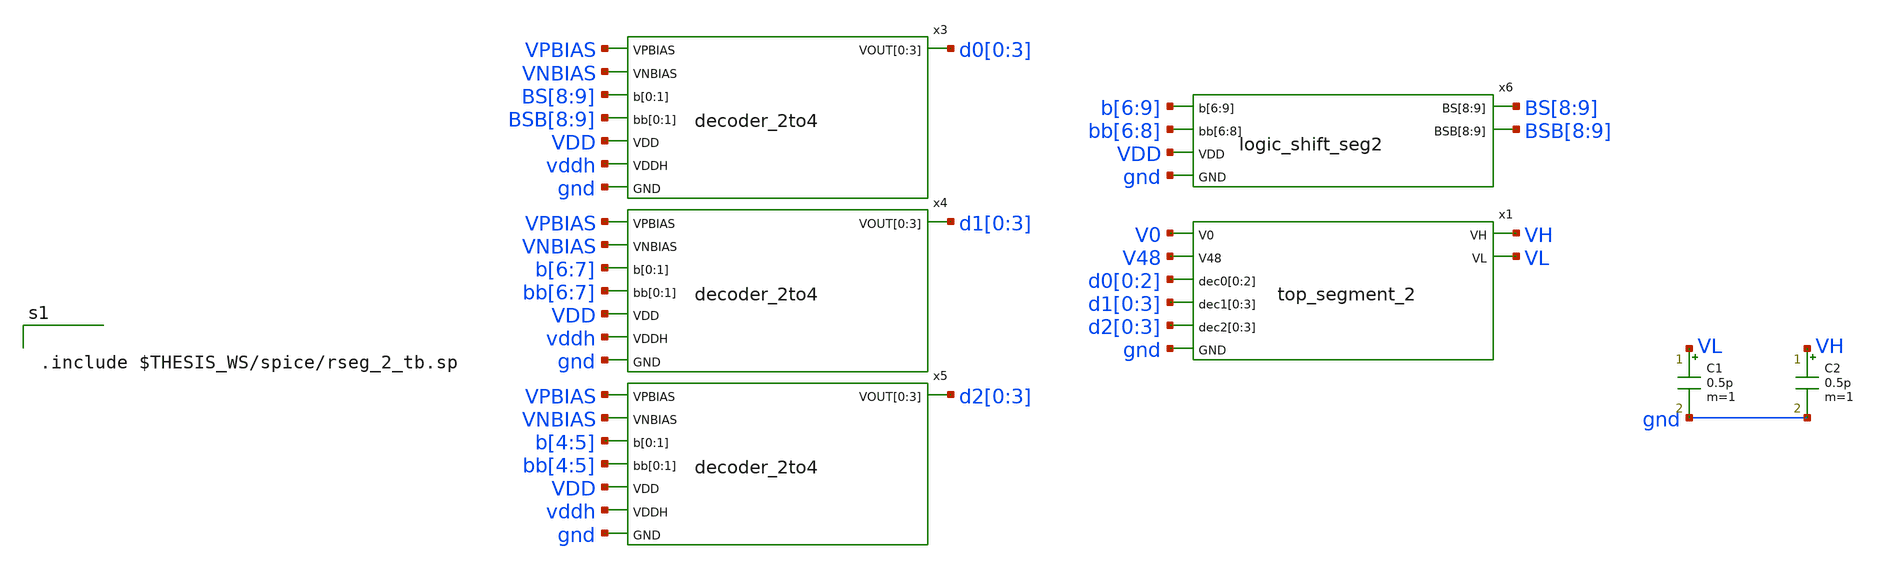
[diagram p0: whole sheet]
** sch_path: xschem/res_seg_2-tb.sch
.lib $::SKYWATER_MODELS/sky130.lib.spice tt
.include $::SKYWATER_STDCELLS/sky130_fd_sc_hd.spice

**.subckt res_seg_2-tb
x3 VPBIAS VNBIAS BS[8] BS[9] BSB[8] BSB[9] d0[0] d0[1] d0[2] d0[3] VDD vddh gnd decoder_2to4
x4 VPBIAS VNBIAS b[6] b[7] bb[6] bb[7] d1[0] d1[1] d1[2] d1[3] VDD vddh gnd decoder_2to4
x5 VPBIAS VNBIAS b[4] b[5] bb[4] bb[5] d2[0] d2[1] d2[2] d2[3] VDD vddh gnd decoder_2to4
x6 b[6] b[7] b[8] b[9] bb[6] bb[7] bb[8] BS[8] BS[9] BSB[8] BSB[9] VDD gnd logic_shift_seg2
x1 V0 V48 d0[0] d0[1] d0[2] d1[0] d1[1] d1[2] d1[3] d2[0] d2[1] d2[2] d2[3] VH VL gnd top_segment_2
C1 VL gnd 0.5p m=1
C2 VH gnd 0.5p m=1
**** begin user architecture code


.include $THESIS_WS/spice/rseg_2_tb.sp


**** end user architecture code
**.ends

* expanding   symbol:  decoder_2to4.sym # of pins=8
** sym_path: xschem/decoder_2to4.sym
** sch_path: xschem/decoder_2to4.sch
.subckt decoder_2to4 VPBIAS VNBIAS b[0] b[1] bb[0] bb[1] VOUT[0] VOUT[1] VOUT[2] VOUT[3] VDD VDDH
+ GND
*.ipin VPBIAS
*.ipin VNBIAS
*.ipin b[0],b[1]
*.opin VOUT[0],VOUT[1],VOUT[2],VOUT[3]
*.ipin VDDH
*.ipin GND
*.ipin VDD
*.ipin bb[0],bb[1]
x1 VPBIAS VNBIAS DIN[0] VOUT[1] VOUT[2] VOUT[3] VOUT[0] VDDH GND VDDH GND pull_up_down_network
x2 VPBIAS VNBIAS DIN[1] VOUT[0] VOUT[2] VOUT[3] VOUT[1] VDDH GND VDDH GND pull_up_down_network
x3 VPBIAS VNBIAS DIN[2] VOUT[0] VOUT[1] VOUT[3] VOUT[2] VDDH GND VDDH GND pull_up_down_network
x4 VPBIAS VNBIAS DIN[3] VOUT[0] VOUT[1] VOUT[2] VOUT[3] VDDH GND VDDH GND pull_up_down_network
x6 bb[1] bb[0] GND GND VDD VDD DIN[0] sky130_fd_sc_hd__nand2_1
x7 b[0] bb[1] GND GND VDD VDD DIN[1] sky130_fd_sc_hd__nand2_1
x8 b[1] bb[0] GND GND VDD VDD DIN[2] sky130_fd_sc_hd__nand2_1
x9 b[0] b[1] GND GND VDD VDD DIN[3] sky130_fd_sc_hd__nand2_1
.ends


* expanding   symbol:  logic_shift_seg2.sym # of pins=6
** sym_path: xschem/logic_shift_seg2.sym
** sch_path: xschem/logic_shift_seg2.sch
.subckt logic_shift_seg2 b[6] b[7] b[8] b[9] bb[6] bb[7] bb[8] BS[8] BS[9] BSB[8] BSB[9] VDD GND
*.ipin b[6],b[7],b[8],b[9]
*.opin BS[8],BS[9]
*.ipin GND
*.ipin VDD
*.ipin bb[6],bb[7],bb[8]
*.opin BSB[8],BSB[9]
x1 b[9] b[8] GND GND VDD VDD n1 sky130_fd_sc_hd__nand2_1
x2 b[7] b[9] GND GND VDD VDD n2 sky130_fd_sc_hd__nand2_1
x3 b[6] b[9] GND GND VDD VDD n3 sky130_fd_sc_hd__nand2_1
x5 bb[6] bb[7] bb[8] GND GND VDD VDD n6 sky130_fd_sc_hd__nand3_1
x4 n1 n3 n2 GND GND VDD VDD BS[9] sky130_fd_sc_hd__nand3_1
x6 b[6] b[8] GND GND VDD VDD n4 sky130_fd_sc_hd__nand2_1
x7 b[8] b[7] GND GND VDD VDD n5 sky130_fd_sc_hd__nand2_1
x8 n6 n5 n4 GND GND VDD VDD BS[8] sky130_fd_sc_hd__nand3_1
x9 BS[9] GND GND VDD VDD BSB[9] sky130_fd_sc_hd__inv_1
x10 BS[8] GND GND VDD VDD BSB[8] sky130_fd_sc_hd__inv_1
.ends


* expanding   symbol:  top_segment_2.sym # of pins=8
** sym_path: xschem/top_segment_2.sym
** sch_path: xschem/top_segment_2.sch
.subckt top_segment_2 V0 V48 dec0[0] dec0[1] dec0[2] dec1[0] dec1[1] dec1[2] dec1[3] dec2[0] dec2[1]
+ dec2[2] dec2[3] VH VL GND
*.ipin V48
*.opin VH
*.ipin GND
*.ipin dec0[0],dec0[1],dec0[2]
*.opin VL
*.ipin dec1[0],dec1[1],dec1[2],dec1[3]
*.ipin dec2[0],dec2[1],dec2[2],dec2[3]
*.ipin V0
x1 V0 V1 V2 V3 V4 V5 V6 V7 V8 V9 V10 V11 V12 V13 V14 V15 V16 V17 V18 V19 V20 V21 V22 V23 V24 V25 V26
+ V27 V28 V29 V30 V31 V32 V33 V34 V35 V36 V37 V38 V39 V40 V41 V42 V43 V44 V45 V46 V47 V48 V0 V1 V2 V3
+ dec0[0] dec0[1] dec0[2] dec0[0] dec0[1] vout1[0] vout1[1] vout1[2] vout1[3] vout1[4] vout1[5] vout1[6]
+ vout1[7] vout1[8] vout1[9] vout1[10] vout1[11] vout1[12] vout1[13] vout1[14] vout1[15] vout1[16] GND
+ vselector_6b_2v_stage_1
x2 vout1[0] vout1[1] vout1[2] vout1[3] vout1[4] vout1[5] vout1[6] vout1[7] vout1[8] vout1[9]
+ vout1[10] vout1[11] vout1[12] vout1[13] vout1[14] vout1[15] vout1[16] dec1[1] dec1[2] dec1[3] dec1[0]
+ vout2[0] vout2[1] vout2[2] vout2[3] vout2[4] GND vselector_6b_2v_stage_2
x3 vout2[0] vout2[1] vout2[2] vout2[3] vout2[4] dec2[0] dec2[1] dec2[2] dec2[3] VH VL GND
+ vselector_6b_2v_stage_3
.param wp=0.42 wn=0.42 l=0.5

x4 V0 V1 V2 V3 V4 V5 V6 V7 V8 V9 V10 V11 V12 V13 V14 V15 V16 V17 V18 V19 V20 V21 V22 V23 V24 V25 V26
+ V27 V28 V29 V30 V31 V32 V33 V34 V35 V36 V37 V38 V39 V40 V41 V42 V43 V44 V45 V46 V47 V48 GND rseg_2_v3
.ends


* expanding   symbol:  pull_up_down_network.sym # of pins=9
** sym_path: xschem/pull_up_down_network.sym
** sch_path: xschem/pull_up_down_network.sch
.subckt pull_up_down_network VPBIAS VNBIAS DIN V[0] V[1] V[2] VOUT VDDH GND VPB VNB
*.ipin VPBIAS
*.ipin VNBIAS
*.ipin DIN
*.ipin V[0],V[1],V[2]
*.opin VOUT
*.ipin VDDH
*.ipin GND
*.ipin VPB
*.ipin VNB
XM1 net2 VPBIAS VDDH VPB sky130_fd_pr__pfet_g5v0d10v5 L=l W=wp nf=1 ad='int((nf+1)/2) * W/nf * 0.29'
+ as='int((nf+2)/2) * W/nf * 0.29' pd='2*int((nf+1)/2) * (W/nf + 0.29)' ps='2*int((nf+2)/2) * (W/nf + 0.29)'
+ nrd='0.29 / W' nrs='0.29 / W' sa=0 sb=0 sd=0 mult=1 m=1
.param wp=0.84 wn=1 l=1

XM2 net3 V[0] net2 VPB sky130_fd_pr__pfet_g5v0d10v5 L=l W=wp nf=1 ad='int((nf+1)/2) * W/nf * 0.29' as='int((nf+2)/2) * W/nf * 0.29'
+ pd='2*int((nf+1)/2) * (W/nf + 0.29)' ps='2*int((nf+2)/2) * (W/nf + 0.29)' nrd='0.29 / W' nrs='0.29 / W'
+ sa=0 sb=0 sd=0 mult=1 m=1
XM3 net4 V[1] net3 VPB sky130_fd_pr__pfet_g5v0d10v5 L=l W=wp nf=1 ad='int((nf+1)/2) * W/nf * 0.29' as='int((nf+2)/2) * W/nf * 0.29'
+ pd='2*int((nf+1)/2) * (W/nf + 0.29)' ps='2*int((nf+2)/2) * (W/nf + 0.29)' nrd='0.29 / W' nrs='0.29 / W'
+ sa=0 sb=0 sd=0 mult=1 m=1
XM4 VOUT V[2] net4 VPB sky130_fd_pr__pfet_g5v0d10v5 L=l W=wp nf=1 ad='int((nf+1)/2) * W/nf * 0.29' as='int((nf+2)/2) * W/nf * 0.29'
+ pd='2*int((nf+1)/2) * (W/nf + 0.29)' ps='2*int((nf+2)/2) * (W/nf + 0.29)' nrd='0.29 / W' nrs='0.29 / W'
+ sa=0 sb=0 sd=0 mult=1 m=1
XM5 VOUT VNBIAS net1 VNB sky130_fd_pr__nfet_g5v0d10v5 L=l W=wn nf=1 ad='int((nf+1)/2) * W/nf * 0.29'
+ as='int((nf+2)/2) * W/nf * 0.29' pd='2*int((nf+1)/2) * (W/nf + 0.29)' ps='2*int((nf+2)/2) * (W/nf + 0.29)'
+ nrd='0.29 / W' nrs='0.29 / W' sa=0 sb=0 sd=0 mult=1 m=1
XM6 net1 DIN GND VNB sky130_fd_pr__nfet_01v8 L=0.15 W=2 nf=1 ad='int((nf+1)/2) * W/nf * 0.29' as='int((nf+2)/2) * W/nf * 0.29'
+ pd='2*int((nf+1)/2) * (W/nf + 0.29)' ps='2*int((nf+2)/2) * (W/nf + 0.29)' nrd='0.29 / W' nrs='0.29 / W'
+ sa=0 sb=0 sd=0 mult=1 m=1
.ends


* expanding   symbol:  vselector_6b_2v_stage_1.sym # of pins=4
** sym_path: xschem/vselector_6b_2v_stage_1.sym
** sch_path: xschem/vselector_6b_2v_stage_1.sch
.subckt vselector_6b_2v_stage_1 vin[0] vin[1] vin[2] vin[3] vin[4] vin[5] vin[6] vin[7] vin[8]
+ vin[9] vin[10] vin[11] vin[12] vin[13] vin[14] vin[15] vin[16] vin[17] vin[18] vin[19] vin[20] vin[21]
+ vin[22] vin[23] vin[24] vin[25] vin[26] vin[27] vin[28] vin[29] vin[30] vin[31] vin[32] vin[33] vin[34]
+ vin[35] vin[36] vin[37] vin[38] vin[39] vin[40] vin[41] vin[42] vin[43] vin[44] vin[45] vin[46] vin[47]
+ vin[48] vin[49] vin[50] vin[51] vin[52] dec[0] dec[1] dec[2] dec[3] dec[4] vout[0] vout[1] vout[2] vout[3]
+ vout[4] vout[5] vout[6] vout[7] vout[8] vout[9] vout[10] vout[11] vout[12] vout[13] vout[14] vout[15]
+ vout[16] VNB
*.ipin
*+ vin[0],vin[1],vin[2],vin[3],vin[4],vin[5],vin[6],vin[7],vin[8],vin[9],vin[10],vin[11],vin[12],vin[13],vin[14],vin[15],vin[16],vin[17],vin[18],vin[19],vin[20],vin[21],vin[22],vin[23],vin[24],vin[25],vin[26],vin[27],vin[28],vin[29],vin[30],vin[31],vin[32],vin[33],vin[34],vin[35],vin[36],vin[37],vin[38],vin[39],vin[40],vin[41],vin[42],vin[43],vin[44],vin[45],vin[46],vin[47],vin[48],vin[49],vin[50],vin[51],vin[52]
*.opin
*+ vout[0],vout[1],vout[2],vout[3],vout[4],vout[5],vout[6],vout[7],vout[8],vout[9],vout[10],vout[11],vout[12],vout[13],vout[14],vout[15],vout[16]
*.ipin VNB
*.ipin dec[0],dec[1],dec[2],dec[3],dec[4]
x1 vin[0] vin[1] vin[2] vin[3] vin[4] vin[5] vin[6] vin[7] vin[8] vin[9] vin[10] vin[11] vin[12]
+ vin[13] vin[14] vin[15] vin[16] dec[0] vout[0] vout[1] vout[2] vout[3] vout[4] vout[5] vout[6] vout[7]
+ vout[8] vout[9] vout[10] vout[11] vout[12] vout[13] vout[14] vout[15] vout[16] VNB vselector_16b
x2 vin[16] vin[17] vin[18] vin[19] vin[20] vin[21] vin[22] vin[23] vin[24] vin[25] vin[26] vin[27]
+ vin[28] vin[29] vin[30] vin[31] vin[32] dec[1] vout[0] vout[1] vout[2] vout[3] vout[4] vout[5] vout[6]
+ vout[7] vout[8] vout[9] vout[10] vout[11] vout[12] vout[13] vout[14] vout[15] vout[16] VNB vselector_16b
x3 vin[32] vin[33] vin[34] vin[35] vin[36] vin[37] vin[38] vin[39] vin[40] vin[41] vin[42] vin[43]
+ vin[44] vin[45] vin[46] vin[47] vin[48] dec[2] vout[0] vout[1] vout[2] vout[3] vout[4] vout[5] vout[6]
+ vout[7] vout[8] vout[9] vout[10] vout[11] vout[12] vout[13] vout[14] vout[15] vout[16] VNB vselector_16b
x4 vin[48] vin[49] vin[50] vin[51] vin[52] dec[3] vout[0] vout[1] vout[2] vout[3] vout[4] VNB
+ vselector_4b
.ends


* expanding   symbol:  vselector_6b_2v_stage_2.sym # of pins=4
** sym_path: xschem/vselector_6b_2v_stage_2.sym
** sch_path: xschem/vselector_6b_2v_stage_2.sch
.subckt vselector_6b_2v_stage_2 vin[0] vin[1] vin[2] vin[3] vin[4] vin[5] vin[6] vin[7] vin[8]
+ vin[9] vin[10] vin[11] vin[12] vin[13] vin[14] vin[15] vin[16] dec[0] dec[1] dec[2] dec[3] vout[0] vout[1]
+ vout[2] vout[3] vout[4] VNB
*.ipin
*+ vin[0],vin[1],vin[2],vin[3],vin[4],vin[5],vin[6],vin[7],vin[8],vin[9],vin[10],vin[11],vin[12],vin[13],vin[14],vin[15],vin[16]
*.opin vout[0],vout[1],vout[2],vout[3],vout[4]
*.ipin VNB
*.ipin dec[0],dec[1],dec[2],dec[3]
x1 vin[0] vin[1] vin[2] vin[3] vin[4] dec[0] vout[0] vout[1] vout[2] vout[3] vout[4] VNB
+ vselector_4b
x2 vin[4] vin[5] vin[6] vin[7] vin[8] dec[1] vout[0] vout[1] vout[2] vout[3] vout[4] VNB
+ vselector_4b
x3 vin[8] vin[9] vin[10] vin[11] vin[12] dec[2] vout[0] vout[1] vout[2] vout[3] vout[4] VNB
+ vselector_4b
x4 vin[12] vin[13] vin[14] vin[15] vin[16] dec[3] vout[0] vout[1] vout[2] vout[3] vout[4] VNB
+ vselector_4b
.ends


* expanding   symbol:  vselector_6b_2v_stage_3.sym # of pins=5
** sym_path: xschem/vselector_6b_2v_stage_3.sym
** sch_path: xschem/vselector_6b_2v_stage_3.sch
.subckt vselector_6b_2v_stage_3 vin[0] vin[1] vin[2] vin[3] vin[4] dec[0] dec[1] dec[2] dec[3] VH VL
+ VNB
*.ipin vin[0],vin[1],vin[2],vin[3],vin[4]
*.opin VH
*.ipin VNB
*.ipin dec[0],dec[1],dec[2],dec[3]
*.opin VL
x1 vin[0] vin[1] dec[0] VH VL VNB vselector_1b
x2 vin[1] vin[2] dec[1] VH VL VNB vselector_1b
x3 vin[2] vin[3] dec[2] VH VL VNB vselector_1b
x4 vin[3] vin[4] dec[3] VH VL VNB vselector_1b
.ends


* expanding   symbol:  vselector_16b.sym # of pins=4
** sym_path: xschem/vselector_16b.sym
** sch_path: xschem/vselector_16b.sch
.subckt vselector_16b vin[0] vin[1] vin[2] vin[3] vin[4] vin[5] vin[6] vin[7] vin[8] vin[9] vin[10]
+ vin[11] vin[12] vin[13] vin[14] vin[15] vin[16] DIN vout[0] vout[1] vout[2] vout[3] vout[4] vout[5] vout[6]
+ vout[7] vout[8] vout[9] vout[10] vout[11] vout[12] vout[13] vout[14] vout[15] vout[16] VNB
*.ipin
*+ vin[0],vin[1],vin[2],vin[3],vin[4],vin[5],vin[6],vin[7],vin[8],vin[9],vin[10],vin[11],vin[12],vin[13],vin[14],vin[15],vin[16]
*.opin
*+ vout[0],vout[1],vout[2],vout[3],vout[4],vout[5],vout[6],vout[7],vout[8],vout[9],vout[10],vout[11],vout[12],vout[13],vout[14],vout[15],vout[16]
*.ipin VNB
*.ipin DIN
XM1 vout[0] DIN vin[0] VNB sky130_fd_pr__nfet_g5v0d10v5 L=l W=wn nf=1 ad='int((nf+1)/2) * W/nf * 0.29'
+ as='int((nf+2)/2) * W/nf * 0.29' pd='2*int((nf+1)/2) * (W/nf + 0.29)' ps='2*int((nf+2)/2) * (W/nf + 0.29)'
+ nrd='0.29 / W' nrs='0.29 / W' sa=0 sb=0 sd=0 mult=1 m=1
XM2 vout[1] DIN vin[1] VNB sky130_fd_pr__nfet_g5v0d10v5 L=l W=wn nf=1 ad='int((nf+1)/2) * W/nf * 0.29'
+ as='int((nf+2)/2) * W/nf * 0.29' pd='2*int((nf+1)/2) * (W/nf + 0.29)' ps='2*int((nf+2)/2) * (W/nf + 0.29)'
+ nrd='0.29 / W' nrs='0.29 / W' sa=0 sb=0 sd=0 mult=1 m=1
XM3 vout[2] DIN vin[2] VNB sky130_fd_pr__nfet_g5v0d10v5 L=l W=wn nf=1 ad='int((nf+1)/2) * W/nf * 0.29'
+ as='int((nf+2)/2) * W/nf * 0.29' pd='2*int((nf+1)/2) * (W/nf + 0.29)' ps='2*int((nf+2)/2) * (W/nf + 0.29)'
+ nrd='0.29 / W' nrs='0.29 / W' sa=0 sb=0 sd=0 mult=1 m=1
XM4 vout[3] DIN vin[3] VNB sky130_fd_pr__nfet_g5v0d10v5 L=l W=wn nf=1 ad='int((nf+1)/2) * W/nf * 0.29'
+ as='int((nf+2)/2) * W/nf * 0.29' pd='2*int((nf+1)/2) * (W/nf + 0.29)' ps='2*int((nf+2)/2) * (W/nf + 0.29)'
+ nrd='0.29 / W' nrs='0.29 / W' sa=0 sb=0 sd=0 mult=1 m=1
XM5 vout[4] DIN vin[4] VNB sky130_fd_pr__nfet_g5v0d10v5 L=l W=wn nf=1 ad='int((nf+1)/2) * W/nf * 0.29'
+ as='int((nf+2)/2) * W/nf * 0.29' pd='2*int((nf+1)/2) * (W/nf + 0.29)' ps='2*int((nf+2)/2) * (W/nf + 0.29)'
+ nrd='0.29 / W' nrs='0.29 / W' sa=0 sb=0 sd=0 mult=1 m=1
XM6 vout[5] DIN vin[5] VNB sky130_fd_pr__nfet_g5v0d10v5 L=l W=wn nf=1 ad='int((nf+1)/2) * W/nf * 0.29'
+ as='int((nf+2)/2) * W/nf * 0.29' pd='2*int((nf+1)/2) * (W/nf + 0.29)' ps='2*int((nf+2)/2) * (W/nf + 0.29)'
+ nrd='0.29 / W' nrs='0.29 / W' sa=0 sb=0 sd=0 mult=1 m=1
XM7 vout[6] DIN vin[6] VNB sky130_fd_pr__nfet_g5v0d10v5 L=l W=wn nf=1 ad='int((nf+1)/2) * W/nf * 0.29'
+ as='int((nf+2)/2) * W/nf * 0.29' pd='2*int((nf+1)/2) * (W/nf + 0.29)' ps='2*int((nf+2)/2) * (W/nf + 0.29)'
+ nrd='0.29 / W' nrs='0.29 / W' sa=0 sb=0 sd=0 mult=1 m=1
XM8 vout[7] DIN vin[7] VNB sky130_fd_pr__nfet_g5v0d10v5 L=l W=wn nf=1 ad='int((nf+1)/2) * W/nf * 0.29'
+ as='int((nf+2)/2) * W/nf * 0.29' pd='2*int((nf+1)/2) * (W/nf + 0.29)' ps='2*int((nf+2)/2) * (W/nf + 0.29)'
+ nrd='0.29 / W' nrs='0.29 / W' sa=0 sb=0 sd=0 mult=1 m=1
XM9 vout[8] DIN vin[8] VNB sky130_fd_pr__nfet_g5v0d10v5 L=l W=wn nf=1 ad='int((nf+1)/2) * W/nf * 0.29'
+ as='int((nf+2)/2) * W/nf * 0.29' pd='2*int((nf+1)/2) * (W/nf + 0.29)' ps='2*int((nf+2)/2) * (W/nf + 0.29)'
+ nrd='0.29 / W' nrs='0.29 / W' sa=0 sb=0 sd=0 mult=1 m=1
XM10 vout[9] DIN vin[9] VNB sky130_fd_pr__nfet_g5v0d10v5 L=l W=wn nf=1 ad='int((nf+1)/2) * W/nf * 0.29'
+ as='int((nf+2)/2) * W/nf * 0.29' pd='2*int((nf+1)/2) * (W/nf + 0.29)' ps='2*int((nf+2)/2) * (W/nf + 0.29)'
+ nrd='0.29 / W' nrs='0.29 / W' sa=0 sb=0 sd=0 mult=1 m=1
XM11 vout[10] DIN vin[10] VNB sky130_fd_pr__nfet_g5v0d10v5 L=l W=wn nf=1 ad='int((nf+1)/2) * W/nf * 0.29'
+ as='int((nf+2)/2) * W/nf * 0.29' pd='2*int((nf+1)/2) * (W/nf + 0.29)' ps='2*int((nf+2)/2) * (W/nf + 0.29)'
+ nrd='0.29 / W' nrs='0.29 / W' sa=0 sb=0 sd=0 mult=1 m=1
XM12 vout[11] DIN vin[11] VNB sky130_fd_pr__nfet_g5v0d10v5 L=l W=wn nf=1 ad='int((nf+1)/2) * W/nf * 0.29'
+ as='int((nf+2)/2) * W/nf * 0.29' pd='2*int((nf+1)/2) * (W/nf + 0.29)' ps='2*int((nf+2)/2) * (W/nf + 0.29)'
+ nrd='0.29 / W' nrs='0.29 / W' sa=0 sb=0 sd=0 mult=1 m=1
XM13 vout[12] DIN vin[12] VNB sky130_fd_pr__nfet_g5v0d10v5 L=l W=wn nf=1 ad='int((nf+1)/2) * W/nf * 0.29'
+ as='int((nf+2)/2) * W/nf * 0.29' pd='2*int((nf+1)/2) * (W/nf + 0.29)' ps='2*int((nf+2)/2) * (W/nf + 0.29)'
+ nrd='0.29 / W' nrs='0.29 / W' sa=0 sb=0 sd=0 mult=1 m=1
XM14 vout[13] DIN vin[13] VNB sky130_fd_pr__nfet_g5v0d10v5 L=l W=wn nf=1 ad='int((nf+1)/2) * W/nf * 0.29'
+ as='int((nf+2)/2) * W/nf * 0.29' pd='2*int((nf+1)/2) * (W/nf + 0.29)' ps='2*int((nf+2)/2) * (W/nf + 0.29)'
+ nrd='0.29 / W' nrs='0.29 / W' sa=0 sb=0 sd=0 mult=1 m=1
XM15 vout[14] DIN vin[14] VNB sky130_fd_pr__nfet_g5v0d10v5 L=l W=wn nf=1 ad='int((nf+1)/2) * W/nf * 0.29'
+ as='int((nf+2)/2) * W/nf * 0.29' pd='2*int((nf+1)/2) * (W/nf + 0.29)' ps='2*int((nf+2)/2) * (W/nf + 0.29)'
+ nrd='0.29 / W' nrs='0.29 / W' sa=0 sb=0 sd=0 mult=1 m=1
XM16 vout[15] DIN vin[15] VNB sky130_fd_pr__nfet_g5v0d10v5 L=l W=wn nf=1 ad='int((nf+1)/2) * W/nf * 0.29'
+ as='int((nf+2)/2) * W/nf * 0.29' pd='2*int((nf+1)/2) * (W/nf + 0.29)' ps='2*int((nf+2)/2) * (W/nf + 0.29)'
+ nrd='0.29 / W' nrs='0.29 / W' sa=0 sb=0 sd=0 mult=1 m=1
XM17 vout[16] DIN vin[16] VNB sky130_fd_pr__nfet_g5v0d10v5 L=l W=wn nf=1 ad='int((nf+1)/2) * W/nf * 0.29'
+ as='int((nf+2)/2) * W/nf * 0.29' pd='2*int((nf+1)/2) * (W/nf + 0.29)' ps='2*int((nf+2)/2) * (W/nf + 0.29)'
+ nrd='0.29 / W' nrs='0.29 / W' sa=0 sb=0 sd=0 mult=1 m=1
.ends


* expanding   symbol:  vselector_4b.sym # of pins=4
** sym_path: xschem/vselector_4b.sym
** sch_path: xschem/vselector_4b.sch
.subckt vselector_4b vin[0] vin[1] vin[2] vin[3] vin[4] DIN vout[0] vout[1] vout[2] vout[3] vout[4]
+ VNB
*.ipin vin[0],vin[1],vin[2],vin[3],vin[4]
*.opin vout[0],vout[1],vout[2],vout[3],vout[4]
*.ipin VNB
*.ipin DIN
XM1 vout[0] DIN vin[0] VNB sky130_fd_pr__nfet_g5v0d10v5 L=l W=wn nf=1 ad='int((nf+1)/2) * W/nf * 0.29'
+ as='int((nf+2)/2) * W/nf * 0.29' pd='2*int((nf+1)/2) * (W/nf + 0.29)' ps='2*int((nf+2)/2) * (W/nf + 0.29)'
+ nrd='0.29 / W' nrs='0.29 / W' sa=0 sb=0 sd=0 mult=1 m=1
XM2 vout[1] DIN vin[1] VNB sky130_fd_pr__nfet_g5v0d10v5 L=l W=wn nf=1 ad='int((nf+1)/2) * W/nf * 0.29'
+ as='int((nf+2)/2) * W/nf * 0.29' pd='2*int((nf+1)/2) * (W/nf + 0.29)' ps='2*int((nf+2)/2) * (W/nf + 0.29)'
+ nrd='0.29 / W' nrs='0.29 / W' sa=0 sb=0 sd=0 mult=1 m=1
XM3 vout[2] DIN vin[2] VNB sky130_fd_pr__nfet_g5v0d10v5 L=l W=wn nf=1 ad='int((nf+1)/2) * W/nf * 0.29'
+ as='int((nf+2)/2) * W/nf * 0.29' pd='2*int((nf+1)/2) * (W/nf + 0.29)' ps='2*int((nf+2)/2) * (W/nf + 0.29)'
+ nrd='0.29 / W' nrs='0.29 / W' sa=0 sb=0 sd=0 mult=1 m=1
XM4 vout[3] DIN vin[3] VNB sky130_fd_pr__nfet_g5v0d10v5 L=l W=wn nf=1 ad='int((nf+1)/2) * W/nf * 0.29'
+ as='int((nf+2)/2) * W/nf * 0.29' pd='2*int((nf+1)/2) * (W/nf + 0.29)' ps='2*int((nf+2)/2) * (W/nf + 0.29)'
+ nrd='0.29 / W' nrs='0.29 / W' sa=0 sb=0 sd=0 mult=1 m=1
XM5 vout[4] DIN vin[4] VNB sky130_fd_pr__nfet_g5v0d10v5 L=l W=wn nf=1 ad='int((nf+1)/2) * W/nf * 0.29'
+ as='int((nf+2)/2) * W/nf * 0.29' pd='2*int((nf+1)/2) * (W/nf + 0.29)' ps='2*int((nf+2)/2) * (W/nf + 0.29)'
+ nrd='0.29 / W' nrs='0.29 / W' sa=0 sb=0 sd=0 mult=1 m=1
.ends


* expanding   symbol:  vselector_1b.sym # of pins=5
** sym_path: xschem/vselector_1b.sym
** sch_path: xschem/vselector_1b.sch
.subckt vselector_1b vin[0] vin[1] DIN VH VL VNB
*.ipin vin[0],vin[1]
*.opin VL
*.ipin VNB
*.ipin DIN
*.opin VH
.param wp=0.42 wn=0.42 l=0.5

XM1 VL DIN vin[0] VNB sky130_fd_pr__nfet_g5v0d10v5 L=l W=wn nf=1 ad='int((nf+1)/2) * W/nf * 0.29' as='int((nf+2)/2) * W/nf * 0.29'
+ pd='2*int((nf+1)/2) * (W/nf + 0.29)' ps='2*int((nf+2)/2) * (W/nf + 0.29)' nrd='0.29 / W' nrs='0.29 / W'
+ sa=0 sb=0 sd=0 mult=1 m=1
XM2 VH DIN vin[1] VNB sky130_fd_pr__nfet_g5v0d10v5 L=l W=wn nf=1 ad='int((nf+1)/2) * W/nf * 0.29' as='int((nf+2)/2) * W/nf * 0.29'
+ pd='2*int((nf+1)/2) * (W/nf + 0.29)' ps='2*int((nf+2)/2) * (W/nf + 0.29)' nrd='0.29 / W' nrs='0.29 / W'
+ sa=0 sb=0 sd=0 mult=1 m=1
.ends

.end
